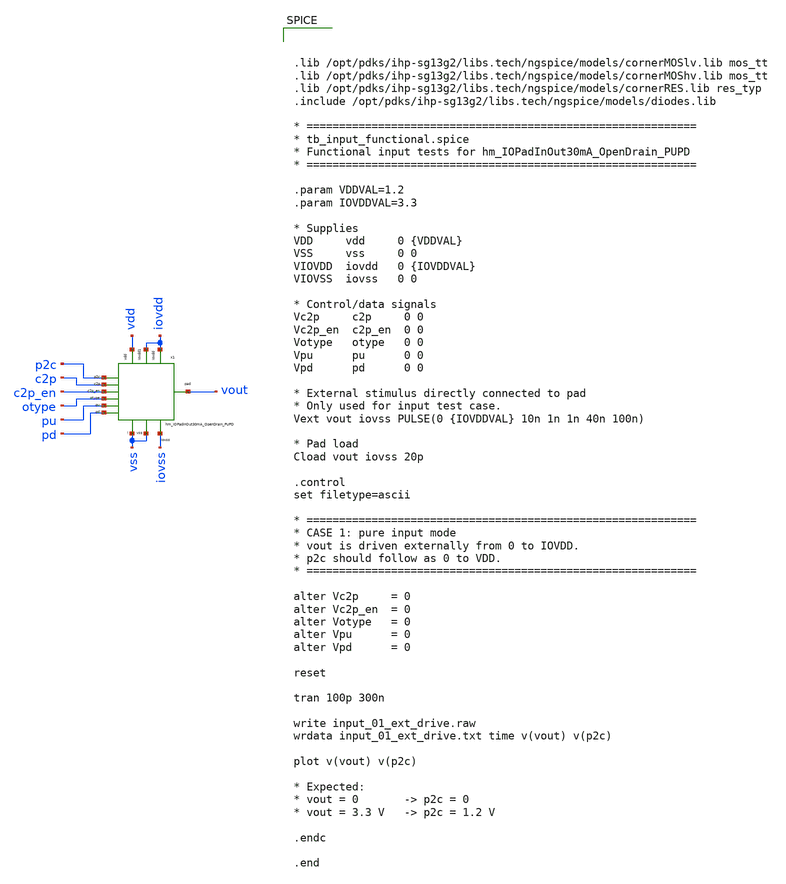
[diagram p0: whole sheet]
** sch_path: ihp-sg13g2/libs.tech/xschem/tests/tb_imode_hm_IOPadInOut30mA_OpenDrain_PUPD.sch
**.subckt tb_imode_hm_IOPadInOut30mA_OpenDrain_PUPD
x1 iovdd iovdd vdd pu c2p vout c2p_en pd otype p2c vss vss iovss hm_IOPadInOut30mA_OpenDrain_PUPD
**** begin user architecture code



.lib /opt/pdks/ihp-sg13g2/libs.tech/ngspice/models/cornerMOSlv.lib mos_tt
.lib /opt/pdks/ihp-sg13g2/libs.tech/ngspice/models/cornerMOShv.lib mos_tt
.lib /opt/pdks/ihp-sg13g2/libs.tech/ngspice/models/cornerRES.lib res_typ
.include /opt/pdks/ihp-sg13g2/libs.tech/ngspice/models/diodes.lib

* ============================================================
* tb_input_functional.spice
* Functional input tests for hm_IOPadInOut30mA_OpenDrain_PUPD
* ============================================================

.param VDDVAL=1.2
.param IOVDDVAL=3.3

* Supplies
VDD     vdd     0 {VDDVAL}
VSS     vss     0 0
VIOVDD  iovdd   0 {IOVDDVAL}
VIOVSS  iovss   0 0

* Control/data signals
Vc2p     c2p     0 0
Vc2p_en  c2p_en  0 0
Votype   otype   0 0
Vpu      pu      0 0
Vpd      pd      0 0

* External stimulus directly connected to pad
* Only used for input test case.
Vext vout iovss PULSE(0 {IOVDDVAL} 10n 1n 1n 40n 100n)

* Pad load
Cload vout iovss 20p

.control
set filetype=ascii

* ============================================================
* CASE 1: pure input mode
* vout is driven externally from 0 to IOVDD.
* p2c should follow as 0 to VDD.
* ============================================================

alter Vc2p     = 0
alter Vc2p_en  = 0
alter Votype   = 0
alter Vpu      = 0
alter Vpd      = 0

reset

tran 100p 300n

write input_01_ext_drive.raw
wrdata input_01_ext_drive.txt time v(vout) v(p2c)

plot v(vout) v(p2c)

* Expected:
* vout = 0       -> p2c = 0
* vout = 3.3 V   -> p2c = 1.2 V

.endc

.end




**** end user architecture code
**.ends
.end
